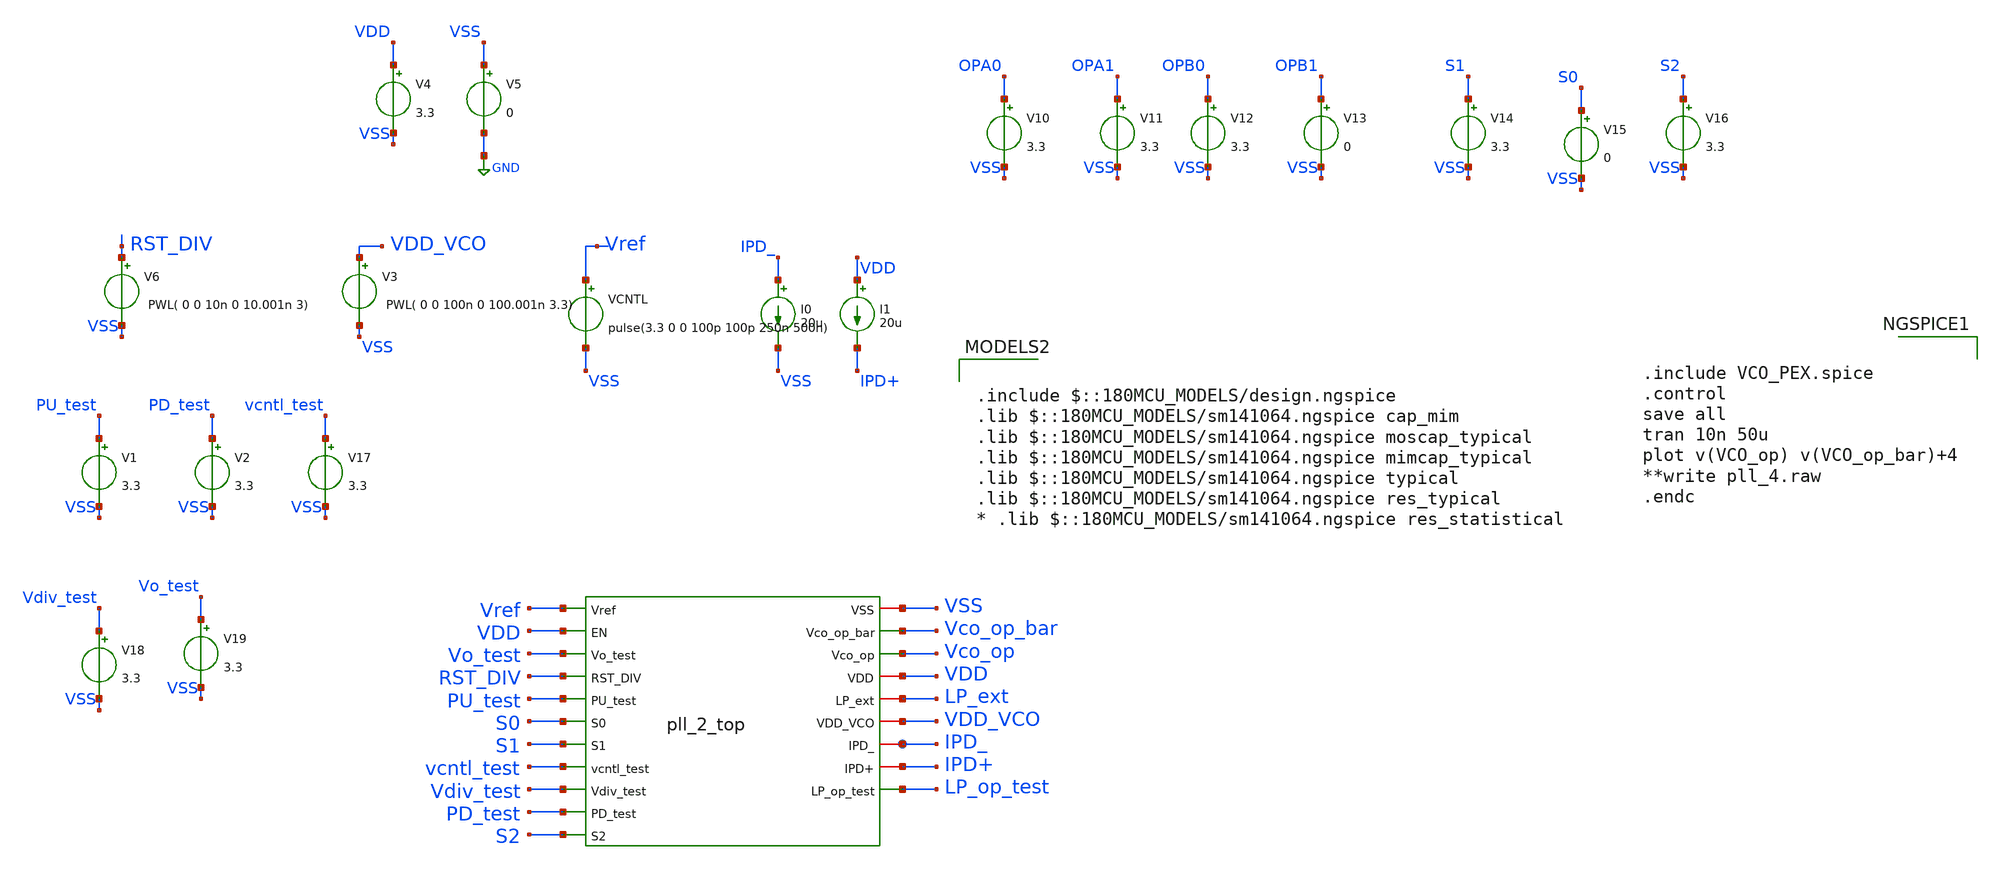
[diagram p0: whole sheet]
** sch_path: Clock_Generator_PAKISTAN_02/Schematics/pll_2_top_TB.sch
**.subckt pll_2_top_TB
VCNTL Vref VSS pulse(3.3 0 0 100p 100p 250n 500n)
V3 VDD_VCO VSS PWL( 0 0 100n 0 100.001n 3.3)
V4 VDD VSS 3.3
V5 VSS GND 0
V6 RST_DIV VSS PWL( 0 0 10n 0 10.001n 3)
V10 OPA0 VSS 3.3
V11 OPA1 VSS 3.3
V12 OPB0 VSS 3.3
V13 OPB1 VSS 0
I0 IPD_ VSS 20u
I1 VDD IPD+ 20u
V14 S1 VSS 3.3
V15 S0 VSS 0
V16 S2 VSS 3.3
V1 PU_test VSS 3.3
V2 PD_test VSS 3.3
V17 vcntl_test VSS 3.3
V18 Vdiv_test VSS 3.3
V19 Vo_test VSS 3.3
x1 VSS Vref Vco_op_bar VDD Vco_op VDD LP_ext VDD_VCO IPD_ Vo_test IPD+ RST_DIV PU_test S0 S1
+ LP_op_test vcntl_test Vdiv_test PD_test S2 pll_2_top
**** begin user architecture code


.include VCO_PEX.spice
.control
save all
tran 10n 50u
plot v(VCO_op) v(VCO_op_bar)+4
**write pll_4.raw
.endc



.include $::180MCU_MODELS/design.ngspice
.lib $::180MCU_MODELS/sm141064.ngspice cap_mim
.lib $::180MCU_MODELS/sm141064.ngspice moscap_typical
.lib $::180MCU_MODELS/sm141064.ngspice mimcap_typical
.lib $::180MCU_MODELS/sm141064.ngspice typical
.lib $::180MCU_MODELS/sm141064.ngspice res_typical
* .lib $::180MCU_MODELS/sm141064.ngspice res_statistical

**** end user architecture code
**.ends
.GLOBAL GND
.end
